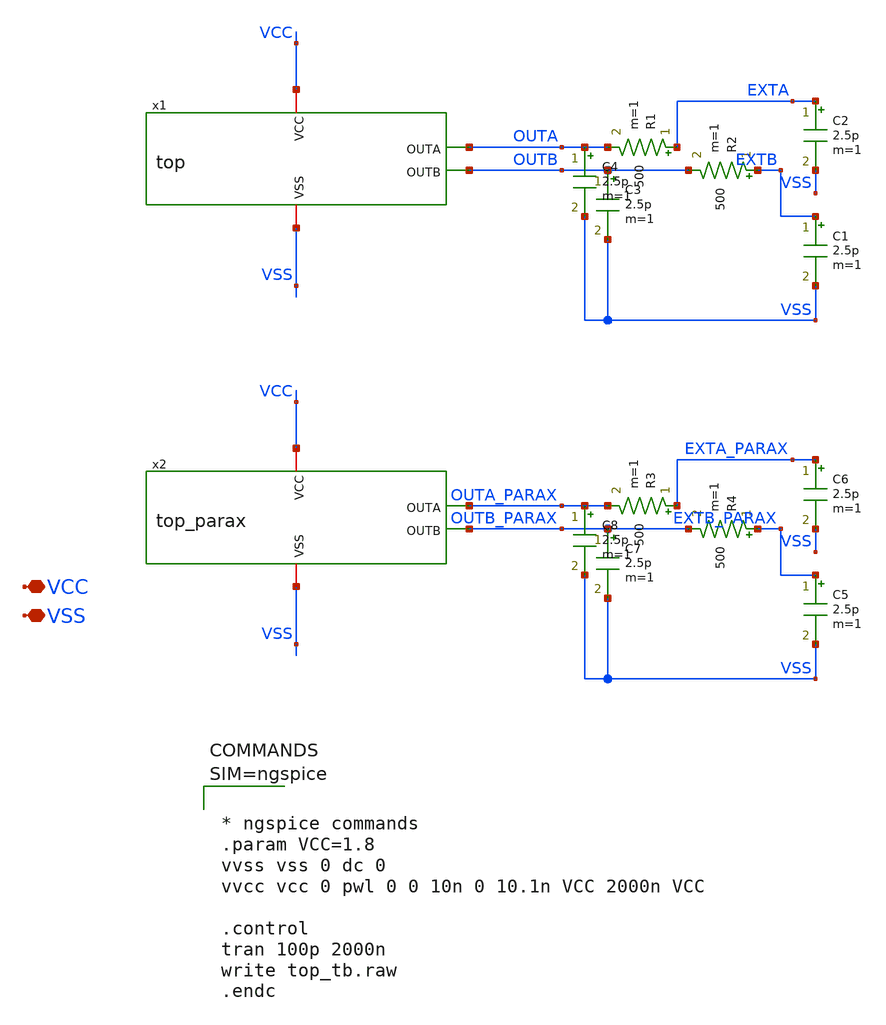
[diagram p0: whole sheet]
** sch_path: xschem/top_tb.sch
**.subckt top_tb VCC VSS
*.iopin VCC
*.iopin VSS
x1 VCC OUTA OUTB VSS top
R1 EXTA OUTA 500 m=1
R2 EXTB OUTB 500 m=1
C1 EXTB VSS 2.5p m=1
C2 EXTA VSS 2.5p m=1
C3 OUTB VSS 2.5p m=1
C4 OUTA VSS 2.5p m=1
x2 VCC OUTA_PARAX OUTB_PARAX VSS top_parax
R3 EXTA_PARAX OUTA_PARAX 500 m=1
R4 EXTB_PARAX OUTB_PARAX 500 m=1
C5 EXTB_PARAX VSS 2.5p m=1
C6 EXTA_PARAX VSS 2.5p m=1
C7 OUTB_PARAX VSS 2.5p m=1
C8 OUTA_PARAX VSS 2.5p m=1
**** begin user architecture code

** opencircuitdesign pdks install
.lib $::SKYWATER_MODELS/sky130.lib.spice tt





* ngspice commands
.param VCC=1.8
vvss vss 0 dc 0
vvcc vcc 0 pwl 0 0 10n 0 10.1n VCC 2000n VCC

.control
tran 100p 2000n
write top_tb.raw
.endc




**** end user architecture code
**.ends

* expanding   symbol:  top.sym # of pins=4
** sym_path: xschem/top.sym
** sch_path: xschem/top.sch
.subckt top VCC OUTA OUTB VSS
*.iopin VCC
*.iopin VSS
*.opin OUTA
*.opin OUTB
x1 VCC OSCA VSS oscillator_20MHZ
x2 VCC OSCB VSS oscillator_21MHZ
x5 VCC VSS IBIAS current_source
x6 VCC FIL_OUTA OSCA_BUF VSS IBIAS filter22M
x7 VCC FIL_OUTB OSCB_BUF VSS IBIAS filter22M
x10 VCC OSCA OSCA_BUF IBIAS VSS analog_buffer
x8 VCC OSCB OSCB_BUF IBIAS VSS analog_buffer
x9 VCC FIL_OUTA OUTA IBIAS VSS analog_buffer
x3 VCC FIL_OUTB OUTB IBIAS VSS analog_buffer
.ends


* expanding   symbol:  top_parax.sym # of pins=4
** sym_path: xschem/top.sym
.include [file normalize ../mag/top.sim.spice]

* expanding   symbol:  oscillator_20MHZ.sym # of pins=3
** sym_path: xschem/oscillator_20MHZ.sym
** sch_path: xschem/oscillator_20MHZ.sch
.subckt oscillator_20MHZ VCC OUT VSS
*.iopin VCC
*.iopin VSS
*.opin OUT
x1[20] INI[19] OUT_INI VCC VSS inverter
x1[19] INI[18] INI[19] VCC VSS inverter
x1[18] INI[17] INI[18] VCC VSS inverter
x1[17] INI[16] INI[17] VCC VSS inverter
x1[16] INI[15] INI[16] VCC VSS inverter
x1[15] INI[14] INI[15] VCC VSS inverter
x1[14] INI[13] INI[14] VCC VSS inverter
x1[13] INI[12] INI[13] VCC VSS inverter
x1[12] INI[11] INI[12] VCC VSS inverter
x1[11] INI[10] INI[11] VCC VSS inverter
x1[10] INI[9] INI[10] VCC VSS inverter
x1[9] INI[8] INI[9] VCC VSS inverter
x1[8] INI[7] INI[8] VCC VSS inverter
x1[7] INI[6] INI[7] VCC VSS inverter
x1[6] INI[5] INI[6] VCC VSS inverter
x1[5] INI[4] INI[5] VCC VSS inverter
x1[4] INI[3] INI[4] VCC VSS inverter
x1[3] INI[2] INI[3] VCC VSS inverter
x1[2] INI[1] INI[2] VCC VSS inverter
x1[1] INI[0] INI[1] VCC VSS inverter
x1[0] OUT_INI INI[0] VCC VSS inverter
x3 OUT OUT_INI VCC VSS inverter
.ends


* expanding   symbol:  oscillator_21MHZ.sym # of pins=3
** sym_path: xschem/oscillator_21MHZ.sym
** sch_path: xschem/oscillator_21MHZ.sch
.subckt oscillator_21MHZ VCC OUT VSS
*.iopin VCC
*.iopin VSS
*.opin OUT
x1[18] INI[17] OUT_INI VCC VSS inverter
x1[17] INI[16] INI[17] VCC VSS inverter
x1[16] INI[15] INI[16] VCC VSS inverter
x1[15] INI[14] INI[15] VCC VSS inverter
x1[14] INI[13] INI[14] VCC VSS inverter
x1[13] INI[12] INI[13] VCC VSS inverter
x1[12] INI[11] INI[12] VCC VSS inverter
x1[11] INI[10] INI[11] VCC VSS inverter
x1[10] INI[9] INI[10] VCC VSS inverter
x1[9] INI[8] INI[9] VCC VSS inverter
x1[8] INI[7] INI[8] VCC VSS inverter
x1[7] INI[6] INI[7] VCC VSS inverter
x1[6] INI[5] INI[6] VCC VSS inverter
x1[5] INI[4] INI[5] VCC VSS inverter
x1[4] INI[3] INI[4] VCC VSS inverter
x1[3] INI[2] INI[3] VCC VSS inverter
x1[2] INI[1] INI[2] VCC VSS inverter
x1[1] INI[0] INI[1] VCC VSS inverter
x1[0] OUT_INI INI[0] VCC VSS inverter
x1 OUT OUT_INI VCC VSS inverter
.ends


* expanding   symbol:  current_source.sym # of pins=3
** sym_path: xschem/current_source.sym
** sch_path: xschem/current_source.sch
.subckt current_source VCC VSS IBIAS
*.iopin VCC
*.iopin VSS
*.opin IBIAS
XM3 IBIAS IBIAS VSS VSS sky130_fd_pr__nfet_01v8 L=1 W=40 nf=1 ad='int((nf+1)/2) * W/nf * 0.29' as='int((nf+2)/2) * W/nf * 0.29'
+ pd='2*int((nf+1)/2) * (W/nf + 0.29)' ps='2*int((nf+2)/2) * (W/nf + 0.29)' nrd='0.29 / W' nrs='0.29 / W'
+ sa=0 sb=0 sd=0 mult=1 m=1
XR1 IBIAS VCC sky130_fd_pr__res_generic_po W=0.33 L=12 m=1
.ends


* expanding   symbol:  filter22M.sym # of pins=5
** sym_path: xschem/filter22M.sym
** sch_path: xschem/filter22M.sch
.subckt filter22M vcc fil_out fil_in vss IBIAS
*.opin fil_out
*.ipin fil_in
*.iopin vcc
*.iopin vss
*.ipin IBIAS
x1 VCC fil_out fil_out op_inb VSS IBIAS opamp_1
XR1 fil_in mid sky130_fd_pr__res_generic_po W=0.5 L=100 m=1
XR2 mid op_inb sky130_fd_pr__res_generic_po W=0.5 L=100 m=1
x2 op_inb mid VSS fil_out capacitor_array
.ends


* expanding   symbol:  analog_buffer.sym # of pins=5
** sym_path: xschem/analog_buffer.sym
** sch_path: xschem/analog_buffer.sch
.subckt analog_buffer VCC BUF_IN BUF_OUT IBIAS VSS
*.ipin BUF_IN
*.iopin VCC
*.iopin VSS
*.ipin IBIAS
*.opin BUF_OUT
x8 VCC BUF_OUT BUF_OUT BUF_IN VSS IBIAS opamp_1
.ends


* expanding   symbol:  inverter.sym # of pins=4
** sym_path: xschem/inverter.sym
** sch_path: xschem/inverter.sch
.subckt inverter OUT IN VCC VSS
*.iopin VCC
*.iopin VSS
*.ipin IN
*.opin OUT
XM1 OUT IN net1 VCC sky130_fd_pr__pfet_01v8 L=1 W=2 nf=1 ad='int((nf+1)/2) * W/nf * 0.29' as='int((nf+2)/2) * W/nf * 0.29'
+ pd='2*int((nf+1)/2) * (W/nf + 0.29)' ps='2*int((nf+2)/2) * (W/nf + 0.29)' nrd='0.29 / W' nrs='0.29 / W'
+ sa=0 sb=0 sd=0 mult=1 m=1
XM2 OUT IN net2 VSS sky130_fd_pr__nfet_01v8 L=1 W=1 nf=1 ad='int((nf+1)/2) * W/nf * 0.29' as='int((nf+2)/2) * W/nf * 0.29'
+ pd='2*int((nf+1)/2) * (W/nf + 0.29)' ps='2*int((nf+2)/2) * (W/nf + 0.29)' nrd='0.29 / W' nrs='0.29 / W'
+ sa=0 sb=0 sd=0 mult=1 m=1
XM3 net1 VSS VCC VCC sky130_fd_pr__pfet_01v8 L=1 W=2 nf=1 ad='int((nf+1)/2) * W/nf * 0.29' as='int((nf+2)/2) * W/nf * 0.29'
+ pd='2*int((nf+1)/2) * (W/nf + 0.29)' ps='2*int((nf+2)/2) * (W/nf + 0.29)' nrd='0.29 / W' nrs='0.29 / W'
+ sa=0 sb=0 sd=0 mult=1 m=1
XM4 net2 VCC VSS VSS sky130_fd_pr__nfet_01v8 L=1 W=1 nf=1 ad='int((nf+1)/2) * W/nf * 0.29' as='int((nf+2)/2) * W/nf * 0.29'
+ pd='2*int((nf+1)/2) * (W/nf + 0.29)' ps='2*int((nf+2)/2) * (W/nf + 0.29)' nrd='0.29 / W' nrs='0.29 / W'
+ sa=0 sb=0 sd=0 mult=1 m=1
.ends


* expanding   symbol:  opamp_1.sym # of pins=6
** sym_path: xschem/opamp_1.sym
** sch_path: xschem/opamp_1.sch
.subckt opamp_1 VCC OUT INA INB VSS IBIAS
*.ipin INA
*.ipin INB
*.opin OUT
*.iopin VCC
*.iopin VSS
*.ipin IBIAS
XM1 MIRR INA TAILV VSS sky130_fd_pr__nfet_01v8 L=1 W=20 nf=1 ad='int((nf+1)/2) * W/nf * 0.29' as='int((nf+2)/2) * W/nf * 0.29'
+ pd='2*int((nf+1)/2) * (W/nf + 0.29)' ps='2*int((nf+2)/2) * (W/nf + 0.29)' nrd='0.29 / W' nrs='0.29 / W'
+ sa=0 sb=0 sd=0 mult=1 m=1
XM2 DIFF_OUT INB TAILV VSS sky130_fd_pr__nfet_01v8 L=1 W=20 nf=1 ad='int((nf+1)/2) * W/nf * 0.29' as='int((nf+2)/2) * W/nf * 0.29'
+ pd='2*int((nf+1)/2) * (W/nf + 0.29)' ps='2*int((nf+2)/2) * (W/nf + 0.29)' nrd='0.29 / W' nrs='0.29 / W'
+ sa=0 sb=0 sd=0 mult=1 m=1
XM3 TAILV IBIAS VSS VSS sky130_fd_pr__nfet_01v8 L=1 W=40 nf=1 ad='int((nf+1)/2) * W/nf * 0.29' as='int((nf+2)/2) * W/nf * 0.29'
+ pd='2*int((nf+1)/2) * (W/nf + 0.29)' ps='2*int((nf+2)/2) * (W/nf + 0.29)' nrd='0.29 / W' nrs='0.29 / W'
+ sa=0 sb=0 sd=0 mult=1 m=1
XM4 MIRR MIRR VCC VCC sky130_fd_pr__pfet_01v8_lvt L=0.5 W=14 nf=1 ad='int((nf+1)/2) * W/nf * 0.29' as='int((nf+2)/2) * W/nf * 0.29'
+ pd='2*int((nf+1)/2) * (W/nf + 0.29)' ps='2*int((nf+2)/2) * (W/nf + 0.29)' nrd='0.29 / W' nrs='0.29 / W'
+ sa=0 sb=0 sd=0 mult=1 m=1
XM5 DIFF_OUT MIRR VCC VCC sky130_fd_pr__pfet_01v8_lvt L=0.5 W=14 nf=1 ad='int((nf+1)/2) * W/nf * 0.29'
+ as='int((nf+2)/2) * W/nf * 0.29' pd='2*int((nf+1)/2) * (W/nf + 0.29)' ps='2*int((nf+2)/2) * (W/nf + 0.29)'
+ nrd='0.29 / W' nrs='0.29 / W' sa=0 sb=0 sd=0 mult=1 m=1
XM6 OUT IBIAS VSS VSS sky130_fd_pr__nfet_01v8 L=0.5 W=93 nf=1 ad='int((nf+1)/2) * W/nf * 0.29' as='int((nf+2)/2) * W/nf * 0.29'
+ pd='2*int((nf+1)/2) * (W/nf + 0.29)' ps='2*int((nf+2)/2) * (W/nf + 0.29)' nrd='0.29 / W' nrs='0.29 / W'
+ sa=0 sb=0 sd=0 mult=1 m=1
XM7 OUT DIFF_OUT VCC VCC sky130_fd_pr__pfet_01v8_lvt L=0.5 W=70 nf=1 ad='int((nf+1)/2) * W/nf * 0.29'
+ as='int((nf+2)/2) * W/nf * 0.29' pd='2*int((nf+1)/2) * (W/nf + 0.29)' ps='2*int((nf+2)/2) * (W/nf + 0.29)'
+ nrd='0.29 / W' nrs='0.29 / W' sa=0 sb=0 sd=0 mult=1 m=1
XM9 RBIAS IBIAS VSS VSS sky130_fd_pr__nfet_01v8 L=1 W=5 nf=1 ad='int((nf+1)/2) * W/nf * 0.29' as='int((nf+2)/2) * W/nf * 0.29'
+ pd='2*int((nf+1)/2) * (W/nf + 0.29)' ps='2*int((nf+2)/2) * (W/nf + 0.29)' nrd='0.29 / W' nrs='0.29 / W'
+ sa=0 sb=0 sd=0 mult=1 m=1
XM10 RBIAS RBIAS net2 VCC sky130_fd_pr__pfet_01v8_lvt L=0.5 W=1 nf=1 ad='int((nf+1)/2) * W/nf * 0.29'
+ as='int((nf+2)/2) * W/nf * 0.29' pd='2*int((nf+1)/2) * (W/nf + 0.29)' ps='2*int((nf+2)/2) * (W/nf + 0.29)'
+ nrd='0.29 / W' nrs='0.29 / W' sa=0 sb=0 sd=0 mult=1 m=1
XM11 net2 net2 VCC VCC sky130_fd_pr__pfet_01v8_lvt L=0.5 W=7.5 nf=1 ad='int((nf+1)/2) * W/nf * 0.29'
+ as='int((nf+2)/2) * W/nf * 0.29' pd='2*int((nf+1)/2) * (W/nf + 0.29)' ps='2*int((nf+2)/2) * (W/nf + 0.29)'
+ nrd='0.29 / W' nrs='0.29 / W' sa=0 sb=0 sd=0 mult=1 m=1
XC1 OUT net1 sky130_fd_pr__cap_mim_m3_2 W=20 L=13 MF=1 m=1
XM8 net1 RBIAS DIFF_OUT VCC sky130_fd_pr__pfet_01v8_lvt L=0.5 W=14 nf=1 ad='int((nf+1)/2) * W/nf * 0.29'
+ as='int((nf+2)/2) * W/nf * 0.29' pd='2*int((nf+1)/2) * (W/nf + 0.29)' ps='2*int((nf+2)/2) * (W/nf + 0.29)'
+ nrd='0.29 / W' nrs='0.29 / W' sa=0 sb=0 sd=0 mult=1 m=1
.ends


* expanding   symbol:  capacitor_array.sym # of pins=4
** sym_path: xschem/capacitor_array.sym
** sch_path: xschem/capacitor_array.sch
.subckt capacitor_array CAPA_P CAPB_P CAPA_N CAPB_N
*.iopin CAPA_P
*.iopin CAPA_N
*.iopin CAPB_P
*.iopin CAPB_N
XC13 CAPA_P CAPA_N sky130_fd_pr__cap_mim_m3_1 W=10 L=6 MF=1 m=1
XC1 CAPA_P CAPA_N sky130_fd_pr__cap_mim_m3_1 W=10 L=6 MF=1 m=1
XC2 CAPA_P CAPA_N sky130_fd_pr__cap_mim_m3_1 W=10 L=6 MF=1 m=1
XC3 CAPA_P CAPA_N sky130_fd_pr__cap_mim_m3_1 W=10 L=6 MF=1 m=1
XC4 CAPB_P CAPB_N sky130_fd_pr__cap_mim_m3_1 W=10 L=6 MF=1 m=1
XC5 CAPB_P CAPB_N sky130_fd_pr__cap_mim_m3_1 W=10 L=6 MF=1 m=1
XC6 CAPB_P CAPB_N sky130_fd_pr__cap_mim_m3_1 W=10 L=6 MF=1 m=1
XC7 CAPB_P CAPB_N sky130_fd_pr__cap_mim_m3_1 W=10 L=6 MF=1 m=1
XC8 CAPB_P CAPB_N sky130_fd_pr__cap_mim_m3_1 W=10 L=6 MF=1 m=1
XC9 CAPB_P CAPB_N sky130_fd_pr__cap_mim_m3_1 W=10 L=6 MF=1 m=1
XC10 CAPB_P CAPB_N sky130_fd_pr__cap_mim_m3_1 W=10 L=6 MF=1 m=1
XC11 CAPB_P CAPB_N sky130_fd_pr__cap_mim_m3_1 W=10 L=6 MF=1 m=1
.ends

.end
